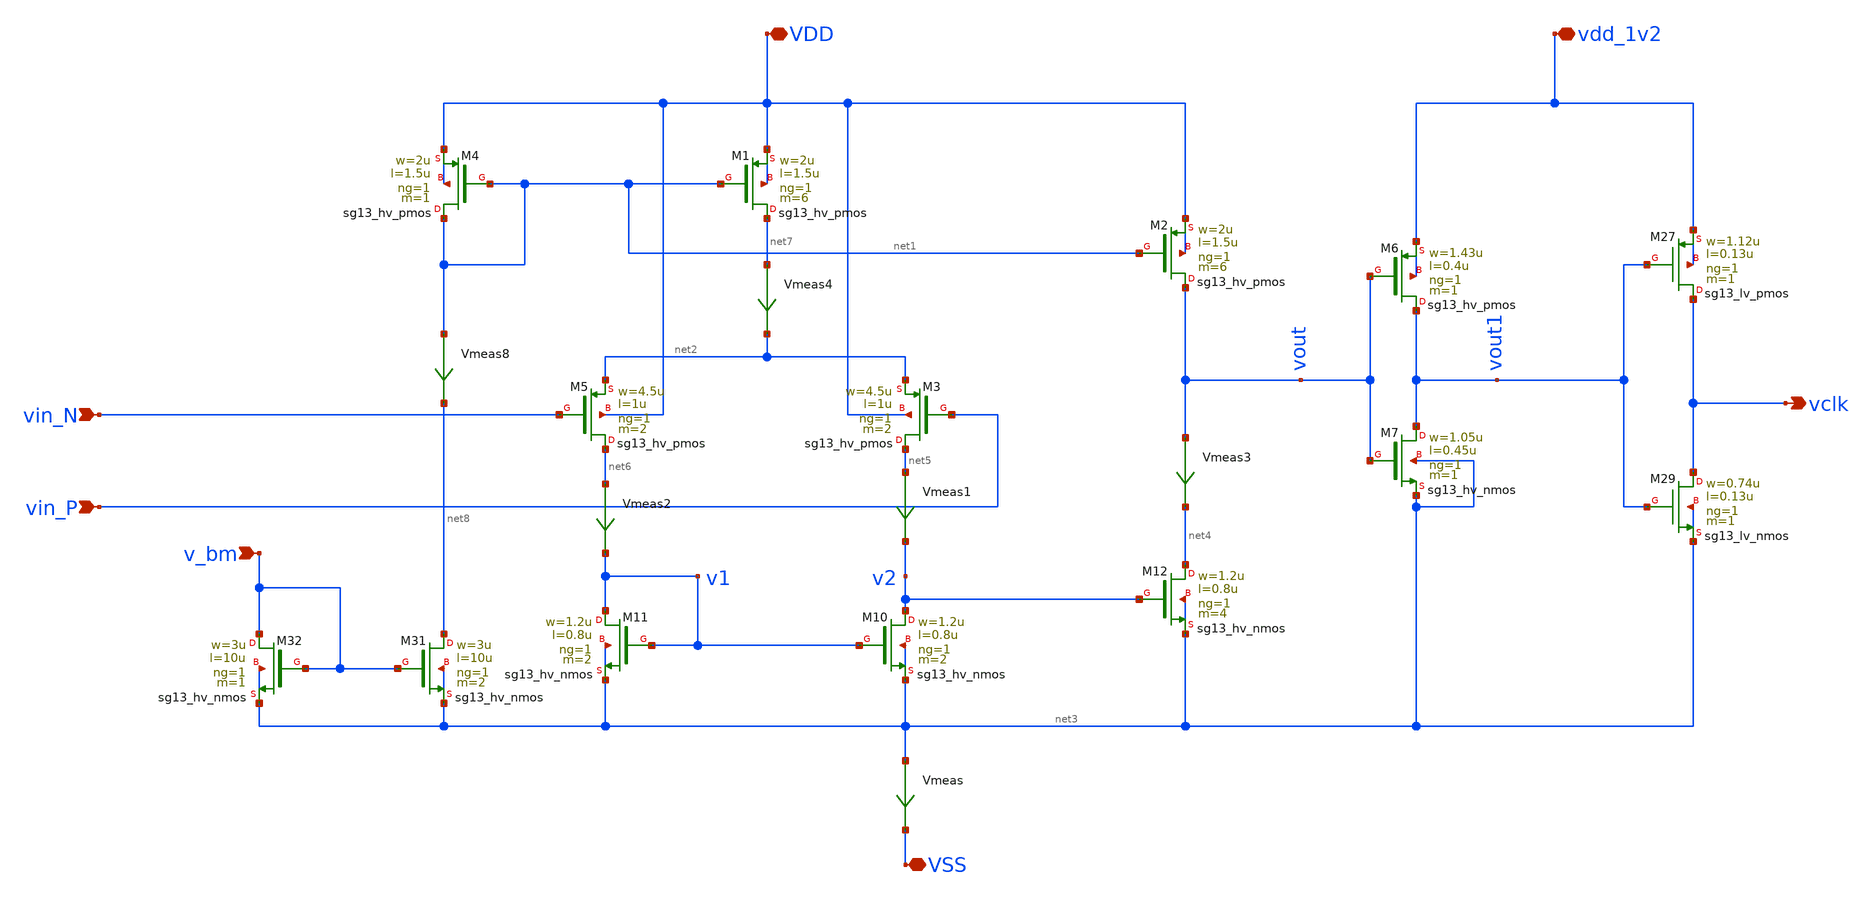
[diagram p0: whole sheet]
** sch_path: dependencies/ClockExtractor/ClockExtractor-main/schematic/xschem/schematic/clock_extractor.sch
**.subckt clock_extractor vin_N vin_P v_bm VDD vdd_1v2 VSS vclk
*.ipin vin_N
*.ipin vin_P
*.ipin v_bm
*.iopin VDD
*.iopin vdd_1v2
*.iopin VSS
*.opin vclk
XM7 vout1 vout net3 net3 sg13_hv_nmos w=1.05u l=0.45u ng=1 m=1 mm_ok=1
XM6 vout1 vout vdd_1v2 vdd_1v2 sg13_hv_pmos w=1.43u l=0.4u ng=1 m=1 mm_ok=1
XM4 net1 net1 VDD VDD sg13_hv_pmos w=2u l=1.5u ng=1 m=1 mm_ok=1
XM1 net7 net1 VDD VDD sg13_hv_pmos w=2u l=1.5u ng=1 m=6 mm_ok=1
XM2 vout net1 VDD VDD sg13_hv_pmos w=2u l=1.5u ng=1 m=6 mm_ok=1
XM3 net5 vin_P net2 VDD sg13_hv_pmos w=4.5u l=1u ng=1 m=2 mm_ok=1
XM5 net6 vin_N net2 VDD sg13_hv_pmos w=4.5u l=1u ng=1 m=2 mm_ok=1
XM10 v2 v1 net3 net3 sg13_hv_nmos w=1.2u l=0.8u ng=1 m=2 mm_ok=1
XM11 v1 v1 net3 net3 sg13_hv_nmos w=1.2u l=0.8u ng=1 m=2 mm_ok=1
XM12 net4 v2 net3 net3 sg13_hv_nmos w=1.2u l=0.8u ng=1 m=4 mm_ok=1
Vmeas net3 VSS 0
.save i(vmeas)
Vmeas1 net5 v2 0
.save i(vmeas1)
Vmeas2 net6 v1 0
.save i(vmeas2)
Vmeas3 vout net4 0
.save i(vmeas3)
Vmeas4 net7 net2 0
.save i(vmeas4)
XM27 vclk vout1 vdd_1v2 vdd_1v2 sg13_lv_pmos w=1.12u l=0.13u ng=1 m=1 mm_ok=1
XM29 vclk vout1 net3 net3 sg13_lv_nmos w=0.74u l=0.13u ng=1 m=1 mm_ok=1
XM31 net8 v_bm net3 net3 sg13_hv_nmos w=3u l=10u ng=1 m=2 mm_ok=1
XM32 v_bm v_bm net3 net3 sg13_hv_nmos w=3u l=10u ng=1 m=1 mm_ok=1
Vmeas8 net1 net8 0
.save i(vmeas8)
**.ends
.end
